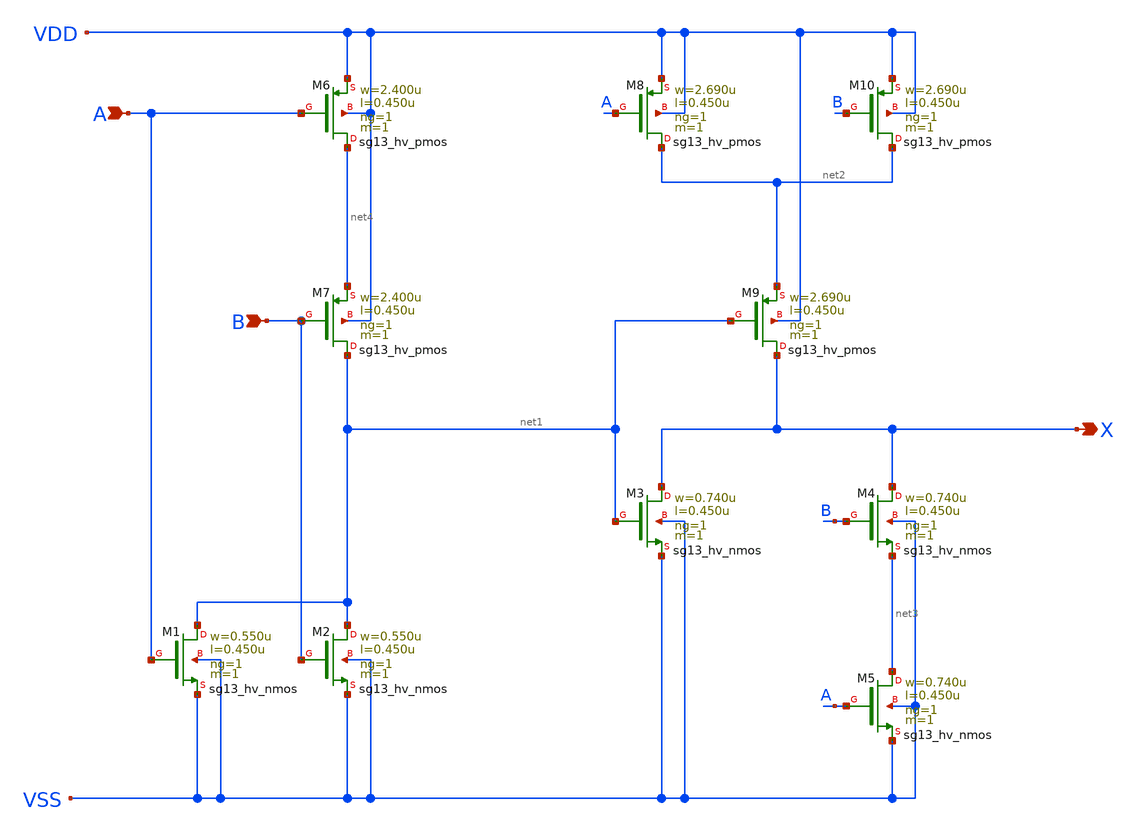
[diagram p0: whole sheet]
** sch_path: ihp-sg13g2/libs.ref/sg13g2_stdcell_hv/sch/xschem/sg13g2_hv_xor2_1.sch
* Copyright 2023 IHP PDK Authors
* Licensed under the Apache License, Version 2.0 (the "License");
* you may not use this file except in compliance with the License.
* You may obtain a copy of the License at
* https://www.apache.org/licenses/LICENSE-2.0
* Unless required by applicable law or agreed to in writing, software
* distributed under the License is distributed on an "AS IS" BASIS,
* WITHOUT WARRANTIES OR CONDITIONS OF ANY KIND, either express or implied.
* See the License for the specific language governing permissions and
* limitations under the License.
**.subckt sg13g2_hv_xor2_1 X B A
*.opin X
*.ipin B
*.ipin A
XM1 net1 A VSS VSS sg13_hv_nmos w=0.550u l=0.450u ng=1 m=1 mm_ok=1
XM2 net1 B VSS VSS sg13_hv_nmos w=0.550u l=0.450u ng=1 m=1 mm_ok=1
XM3 X net1 VSS VSS sg13_hv_nmos w=0.740u l=0.450u ng=1 m=1 mm_ok=1
XM4 X B net3 VSS sg13_hv_nmos w=0.740u l=0.450u ng=1 m=1 mm_ok=1
XM5 net3 A VSS VSS sg13_hv_nmos w=0.740u l=0.450u ng=1 m=1 mm_ok=1
XM6 net4 A VDD VDD sg13_hv_pmos w=2.400u l=0.450u ng=1 m=1 mm_ok=1
XM7 net1 B net4 VDD sg13_hv_pmos w=2.400u l=0.450u ng=1 m=1 mm_ok=1
XM8 net2 A VDD VDD sg13_hv_pmos w=2.690u l=0.450u ng=1 m=1 mm_ok=1
XM9 X net1 net2 VDD sg13_hv_pmos w=2.690u l=0.450u ng=1 m=1 mm_ok=1
XM10 net2 B VDD VDD sg13_hv_pmos w=2.690u l=0.450u ng=1 m=1 mm_ok=1
**.ends
.end
